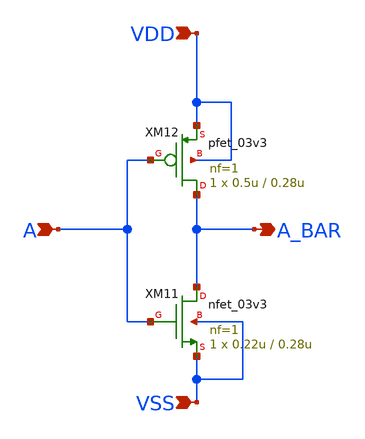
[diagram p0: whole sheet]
** sch_path: designs/INV.sch
**.subckt INV A VDD VSS A_BAR
*.ipin A
*.ipin VDD
*.ipin VSS
*.opin A_BAR
XM11 A_BAR A VSS VSS nfet_03v3 L=0.28u W=0.22u nf=1 ad='int((nf+1)/2) * W/nf * 0.18u' as='int((nf+2)/2) * W/nf * 0.18u'
+ pd='2*int((nf+1)/2) * (W/nf + 0.18u)' ps='2*int((nf+2)/2) * (W/nf + 0.18u)' nrd='0.18u / W' nrs='0.18u / W'
+ sa=0 sb=0 sd=0 m=1
XM12 A_BAR A VDD VDD pfet_03v3 L=0.28u W=0.5u nf=1 ad='int((nf+1)/2) * W/nf * 0.18u' as='int((nf+2)/2) * W/nf * 0.18u'
+ pd='2*int((nf+1)/2) * (W/nf + 0.18u)' ps='2*int((nf+2)/2) * (W/nf + 0.18u)' nrd='0.18u / W' nrs='0.18u / W'
+ sa=0 sb=0 sd=0 m=1
**.ends
.end
